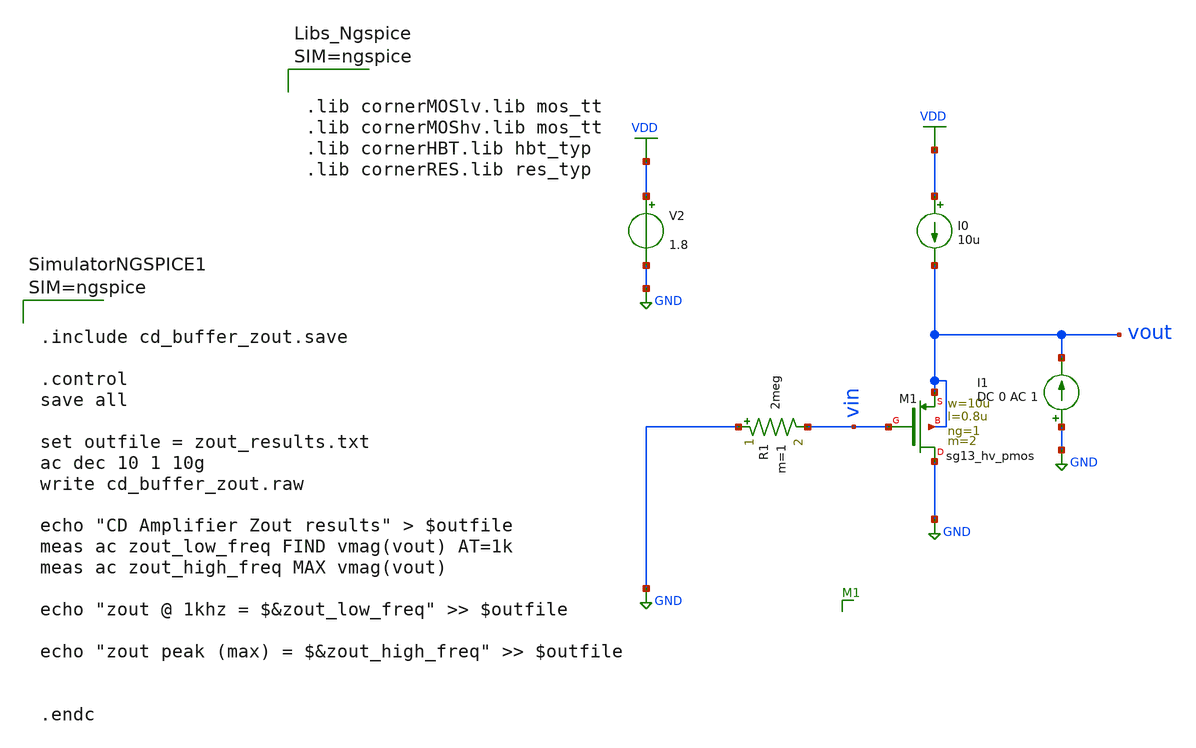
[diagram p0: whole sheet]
** sch_path: Schematics/lab_3/cd_buffer_zout.sch
**.subckt cd_buffer_zout
XM1 GND vin vout vout sg13_hv_pmos w=10u l=0.8u ng=1 m=2 mm_ok=1
R1 GND vin 2meg m=1
I0 VDD vout 10u
V2 VDD GND 1.8
I1 GND vout DC 0 AC 1
**** begin user architecture code



.lib cornerMOSlv.lib mos_tt
.lib cornerMOShv.lib mos_tt
.lib cornerHBT.lib hbt_typ
.lib cornerRES.lib res_typ






.include cd_buffer_zout.save

.control
save all

set outfile = zout_results.txt
ac dec 10 1 10g
write cd_buffer_zout.raw

echo "CD Amplifier Zout results" > $outfile
meas ac zout_low_freq FIND vmag(vout) AT=1k
meas ac zout_high_freq MAX vmag(vout)

echo "zout @ 1khz = $&zout_low_freq" >> $outfile

echo "zout peak (max) = $&zout_high_freq" >> $outfile


.endc



**** end user architecture code
**.ends
.GLOBAL GND
.GLOBAL VDD
.end
